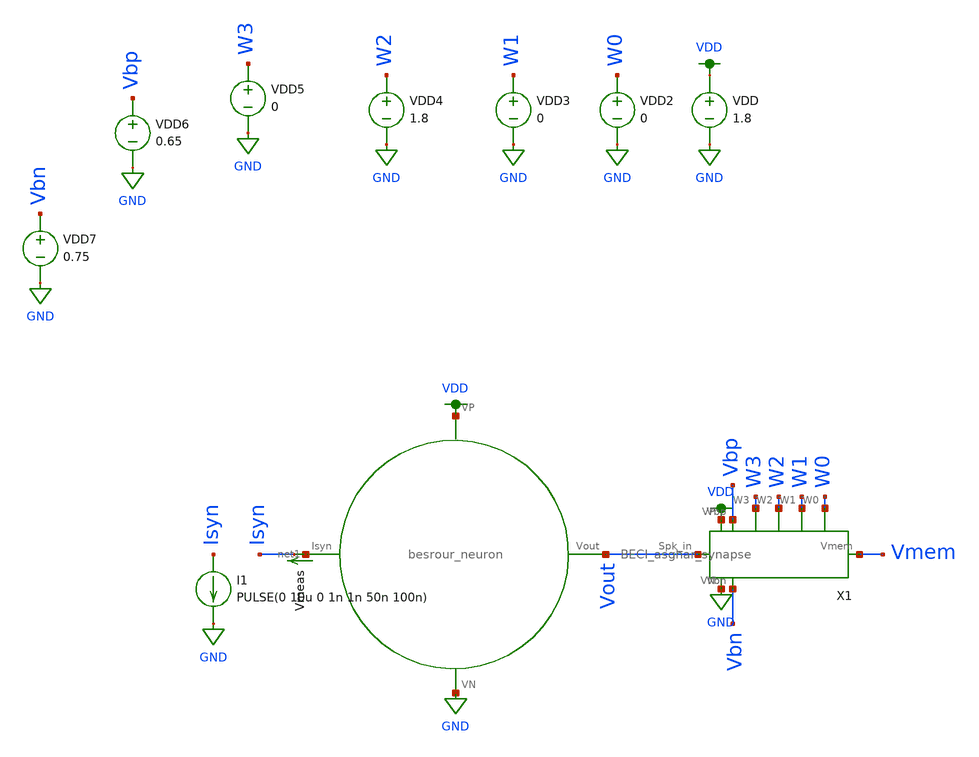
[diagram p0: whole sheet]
** sch_path: schematic/tran_neuron.sch
**.subckt tran_neuron
X1 net1 Vout VDD GND besrour_neuron
VDD VDD GND 1.8
I1 Isyn GND PULSE(0 10u 0 1n 1n 50n 100n)
Vmeas net1 Isyn 0
.save i(vmeas)
VDD2 W0 GND 0
VDD3 W1 GND 0
VDD4 W2 GND 1.8
VDD5 W3 GND 0
VDD6 Vbp GND 0.65
VDD7 Vbn GND 0.75
X1 VDD GND Vout Vmem W3 W2 W1 W0 Vbp Vbn BECI_asghar_synapse
**** begin user architecture code

.param W=12
.param L=0.5
.tran 0.01n 1u
.save all


.option wnflag=1
.param MC_SWITCH=0.0
.lib ~/skywater/skywater-pdk/libraries/sky130_fd_pr_ngspice/latest/models/sky130.lib.spice tt

**** end user architecture code
**.ends
.GLOBAL GND
.GLOBAL VDD
.end
